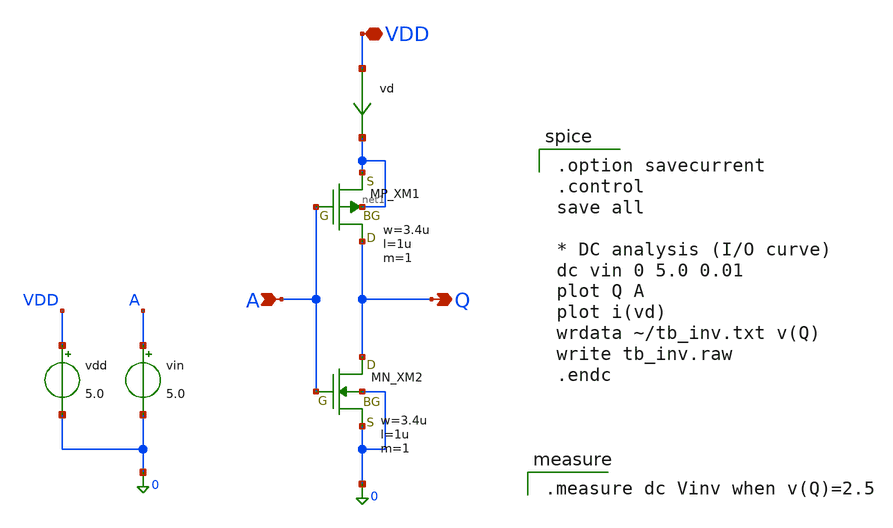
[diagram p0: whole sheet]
** sch_path: member_project/inverter/ZEP/yanzm/tb_inverter_yanzm.sch
**.subckt tb_inverter_yanzm A VDD Q
*.ipin A
*.iopin VDD
*.opin Q
XM1 Q A net1 net1 PMOS w=3.4u l=1u as=0 ad=0 ps=0 pd=0 nrd=0 nrs=0 m=1
XM2 Q A 0 0 NMOS w=3.4u l=1u as=0 ad=0 ps=0 pd=0 nrd=0 nrs=0 m=1
vdd VDD 0 5.0
vin A 0 5.0
vd VDD net1 0
.save i(vd)
**** begin user architecture code
 .include $::LIB/ip62_models

.option savecurrent
.control
save all

* DC analysis (I/O curve)
dc vin 0 5.0 0.01
plot Q A
plot i(vd)
wrdata ~/tb_inv.txt v(Q)
write tb_inv.raw
.endc


.measure dc Vinv when v(Q)=2.5

**** end user architecture code
**.ends
.end
